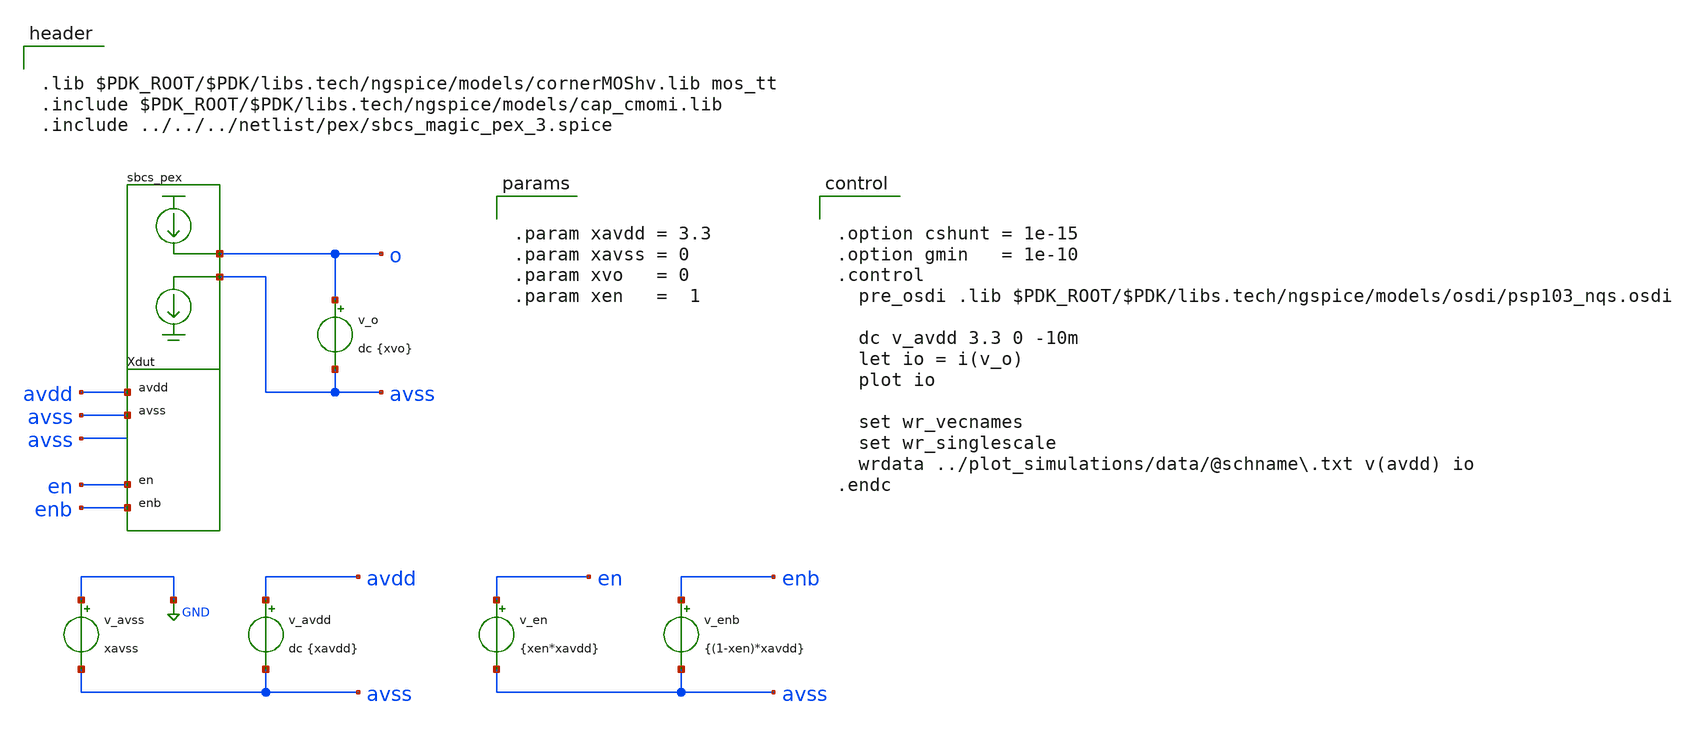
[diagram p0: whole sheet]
** sch_path: macros/sbcs/testbenches/xschem/pex_tb_sbcs_vsweep.sch
**.subckt pex_tb_sbcs_vsweep
Xdut o avss avdd avss en enb sbcs_pex
v_avss GND avss xavss
v_avdd avdd avss dc {xavdd}
v_en en avss {xen*xavdd}
v_enb enb avss {(1-xen)*xavdd}
v_o o avss dc {xvo}
**** begin user architecture code


.lib $PDK_ROOT/$PDK/libs.tech/ngspice/models/cornerMOShv.lib mos_tt
.include $PDK_ROOT/$PDK/libs.tech/ngspice/models/cap_cmomi.lib
.include ../../../netlist/pex/sbcs_magic_pex_3.spice




.option cshunt = 1e-15
.option gmin   = 1e-10
.control
  pre_osdi .lib $PDK_ROOT/$PDK/libs.tech/ngspice/models/osdi/psp103_nqs.osdi

  dc v_avdd 3.3 0 -10m
  let io = i(v_o)
  plot io

  set wr_vecnames
  set wr_singlescale
  wrdata ../plot_simulations/data/@schname\.txt v(avdd) io
.endc




.param xavdd = 3.3
.param xavss = 0
.param xvo   = 0
.param xen   =  1


**** end user architecture code
**.ends
.GLOBAL GND
.end
